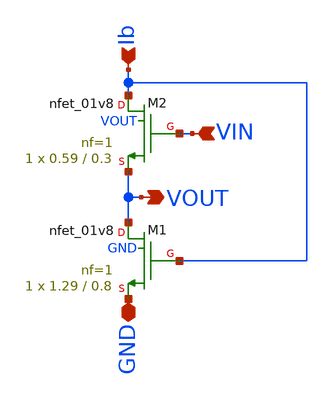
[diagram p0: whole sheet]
** sch_path: xschem/fvf.sch
**.subckt fvf VIN VOUT GND Ib
*.ipin VIN
*.opin VOUT
*.iopin GND
*.ipin Ib
XM1 VOUT Ib GND GND sky130_fd_pr__nfet_01v8 L=0.8 W=1.29 nf=1 ad='int((nf+1)/2) * W/nf * 0.29' as='int((nf+2)/2) * W/nf * 0.29'
+ pd='2*int((nf+1)/2) * (W/nf + 0.29)' ps='2*int((nf+2)/2) * (W/nf + 0.29)' nrd='0.29 / W' nrs='0.29 / W'
+ sa=0 sb=0 sd=0 mult=1 m=1
XM2 Ib VIN VOUT VOUT sky130_fd_pr__nfet_01v8 L=0.3 W=0.59 nf=1 ad='int((nf+1)/2) * W/nf * 0.29' as='int((nf+2)/2) * W/nf * 0.29'
+ pd='2*int((nf+1)/2) * (W/nf + 0.29)' ps='2*int((nf+2)/2) * (W/nf + 0.29)' nrd='0.29 / W' nrs='0.29 / W'
+ sa=0 sb=0 sd=0 mult=1 m=1
**.ends
.end
